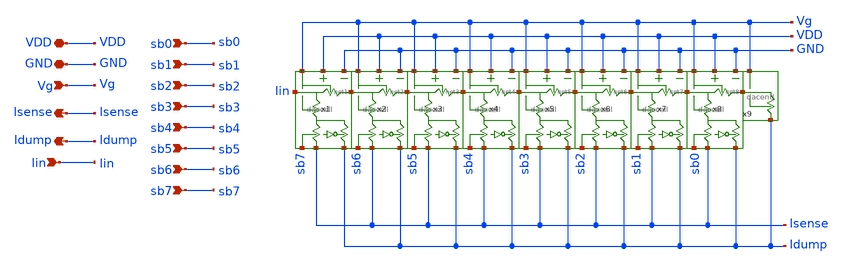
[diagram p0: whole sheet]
** sch_path: final/schematics/dac.sch
**.subckt dac VDD GND sb0 sb1 sb2 sb3 sb4 sb5 sb6 sb7 Isense Idump Vg Iin
*.iopin VDD
*.iopin GND
*.ipin sb0
*.ipin sb1
*.ipin sb2
*.ipin sb3
*.ipin sb4
*.ipin sb5
*.ipin sb6
*.ipin sb7
*.opin Isense
*.opin Idump
*.ipin Vg
*.ipin Iin
x1 net1 GND Iin Vg sb7 Isense VDD Idump daccell
x2 net2 GND net1 Vg sb6 Isense VDD Idump daccell
x3 net3 GND net2 Vg sb5 Isense VDD Idump daccell
x4 net4 GND net3 Vg sb4 Isense VDD Idump daccell
x5 net5 GND net4 Vg sb3 Isense VDD Idump daccell
x6 net6 GND net5 Vg sb2 Isense VDD Idump daccell
x7 net7 GND net6 Vg sb1 Isense VDD Idump daccell
x8 net8 GND net7 Vg sb0 Isense VDD Idump daccell
x9 net8 Vg Idump dacend
**.ends
.end
